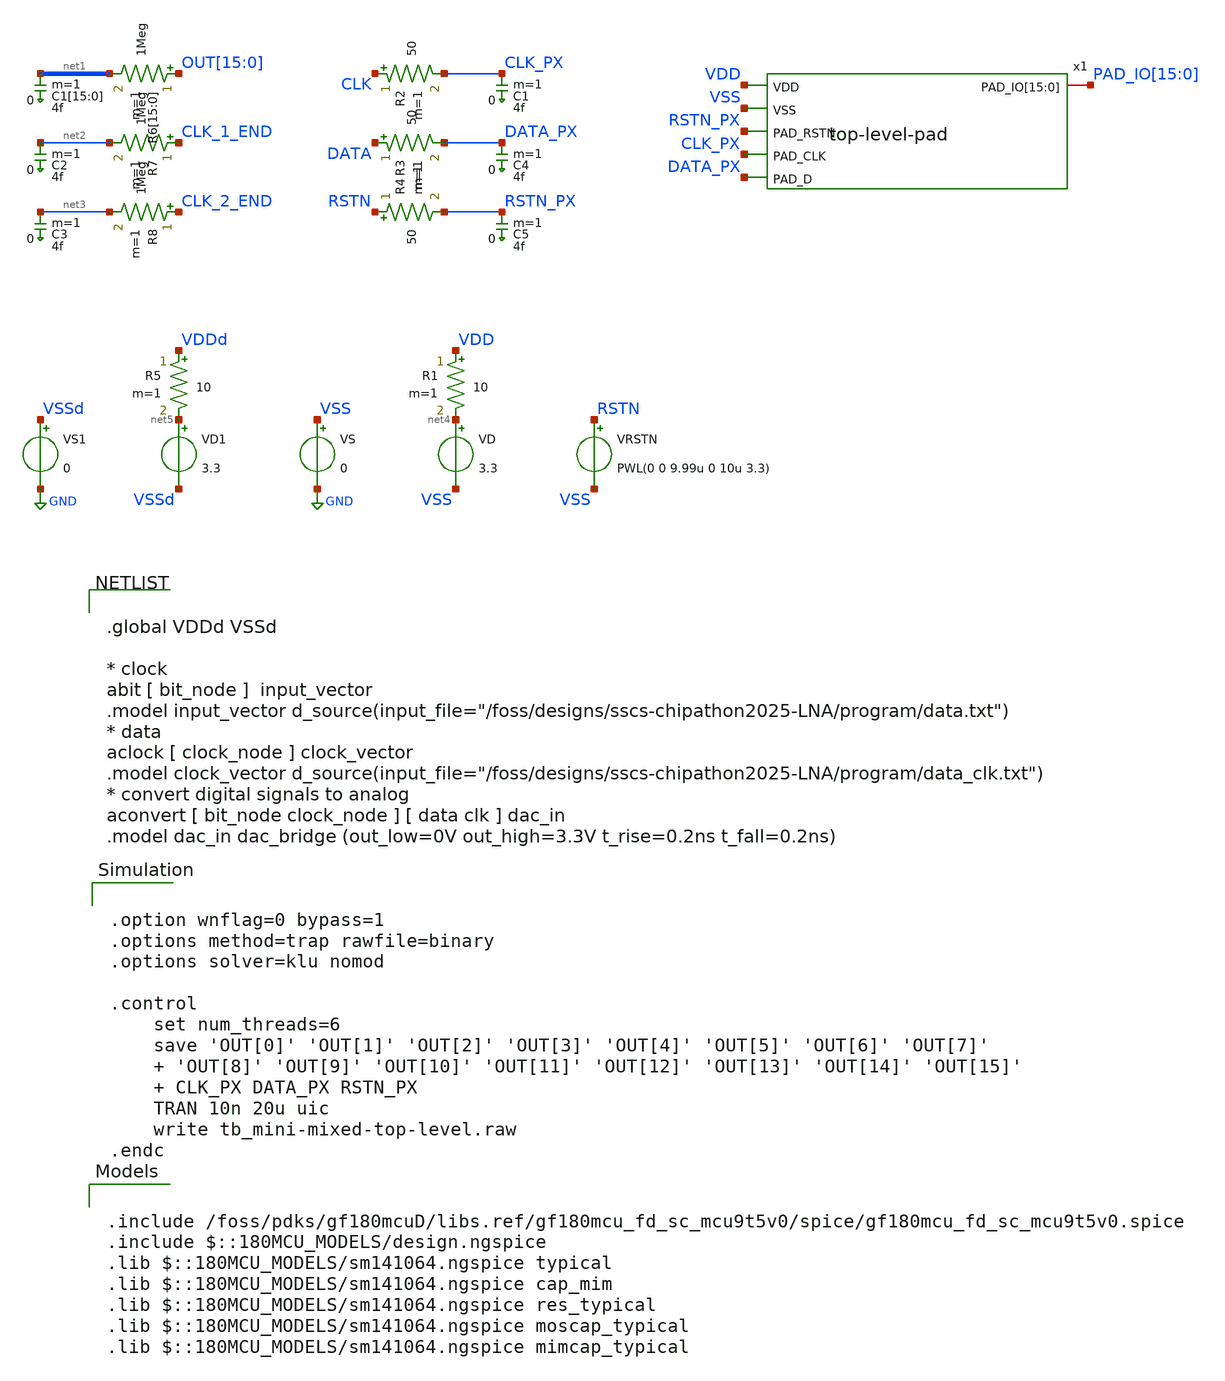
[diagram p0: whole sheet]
** sch_path: designs/libs/tb_top-level/tb_full-top-level.sch
**.subckt tb_full-top-level
VD net4 VSS 3.3
R1 VDD net4 10 m=1
R2 CLK CLK_PX 50 m=1
R3 DATA DATA_PX 50 m=1
VS VSS GND 0
VRSTN RSTN VSS PWL(0 0 9.99u 0 10u 3.3)
R4 RSTN RSTN_PX 50 m=1
VD1 net5 VSSd 3.3
R5 VDDd net5 10 m=1
VS1 VSSd GND 0
C1[15] net1[15] 0 4f m=1
C1[14] net1[14] 0 4f m=1
C1[13] net1[13] 0 4f m=1
C1[12] net1[12] 0 4f m=1
C1[11] net1[11] 0 4f m=1
C1[10] net1[10] 0 4f m=1
C1[9] net1[9] 0 4f m=1
C1[8] net1[8] 0 4f m=1
C1[7] net1[7] 0 4f m=1
C1[6] net1[6] 0 4f m=1
C1[5] net1[5] 0 4f m=1
C1[4] net1[4] 0 4f m=1
C1[3] net1[3] 0 4f m=1
C1[2] net1[2] 0 4f m=1
C1[1] net1[1] 0 4f m=1
C1[0] net1[0] 0 4f m=1
C2 net2 0 4f m=1
C3 net3 0 4f m=1
C1 CLK_PX 0 4f m=1
C4 DATA_PX 0 4f m=1
R6[15] OUT[15] net1[15] 1Meg m=1
R6[14] OUT[14] net1[14] 1Meg m=1
R6[13] OUT[13] net1[13] 1Meg m=1
R6[12] OUT[12] net1[12] 1Meg m=1
R6[11] OUT[11] net1[11] 1Meg m=1
R6[10] OUT[10] net1[10] 1Meg m=1
R6[9] OUT[9] net1[9] 1Meg m=1
R6[8] OUT[8] net1[8] 1Meg m=1
R6[7] OUT[7] net1[7] 1Meg m=1
R6[6] OUT[6] net1[6] 1Meg m=1
R6[5] OUT[5] net1[5] 1Meg m=1
R6[4] OUT[4] net1[4] 1Meg m=1
R6[3] OUT[3] net1[3] 1Meg m=1
R6[2] OUT[2] net1[2] 1Meg m=1
R6[1] OUT[1] net1[1] 1Meg m=1
R6[0] OUT[0] net1[0] 1Meg m=1
R7 CLK_1_END net2 1Meg m=1
R8 CLK_2_END net3 1Meg m=1
C5 RSTN_PX 0 4f m=1
x1 VDD VSS RSTN_PX CLK_PX DATA_PX PAD_IO[15] PAD_IO[14] PAD_IO[13] PAD_IO[12] PAD_IO[11] PAD_IO[10]
+ PAD_IO[9] PAD_IO[8] PAD_IO[7] PAD_IO[6] PAD_IO[5] PAD_IO[4] PAD_IO[3] PAD_IO[2] PAD_IO[1] PAD_IO[0]
+ top-level-pad
**** begin user architecture code


.option wnflag=0 bypass=1
.options method=trap rawfile=binary
.options solver=klu nomod

.control
    set num_threads=6
    save 'OUT[0]' 'OUT[1]' 'OUT[2]' 'OUT[3]' 'OUT[4]' 'OUT[5]' 'OUT[6]' 'OUT[7]'
    + 'OUT[8]' 'OUT[9]' 'OUT[10]' 'OUT[11]' 'OUT[12]' 'OUT[13]' 'OUT[14]' 'OUT[15]'
    + CLK_PX DATA_PX RSTN_PX
    TRAN 10n 20u uic
    write tb_mini-mixed-top-level.raw
.endc



.include /foss/pdks/gf180mcuD/libs.ref/gf180mcu_fd_sc_mcu9t5v0/spice/gf180mcu_fd_sc_mcu9t5v0.spice
.include $::180MCU_MODELS/design.ngspice
.lib $::180MCU_MODELS/sm141064.ngspice typical
.lib $::180MCU_MODELS/sm141064.ngspice cap_mim
.lib $::180MCU_MODELS/sm141064.ngspice res_typical
.lib $::180MCU_MODELS/sm141064.ngspice moscap_typical
.lib $::180MCU_MODELS/sm141064.ngspice mimcap_typical



.global VDDd VSSd

* clock
abit [ bit_node ]  input_vector
.model input_vector d_source(input_file="/foss/designs/sscs-chipathon2025-LNA/program/data.txt")
* data
aclock [ clock_node ] clock_vector
.model clock_vector d_source(input_file="/foss/designs/sscs-chipathon2025-LNA/program/data_clk.txt")
* convert digital signals to analog
aconvert [ bit_node clock_node ] [ data clk ] dac_in
.model dac_in dac_bridge (out_low=0V out_high=3.3V t_rise=0.2ns t_fall=0.2ns)


**** end user architecture code
**.ends
.GLOBAL GND
.end
